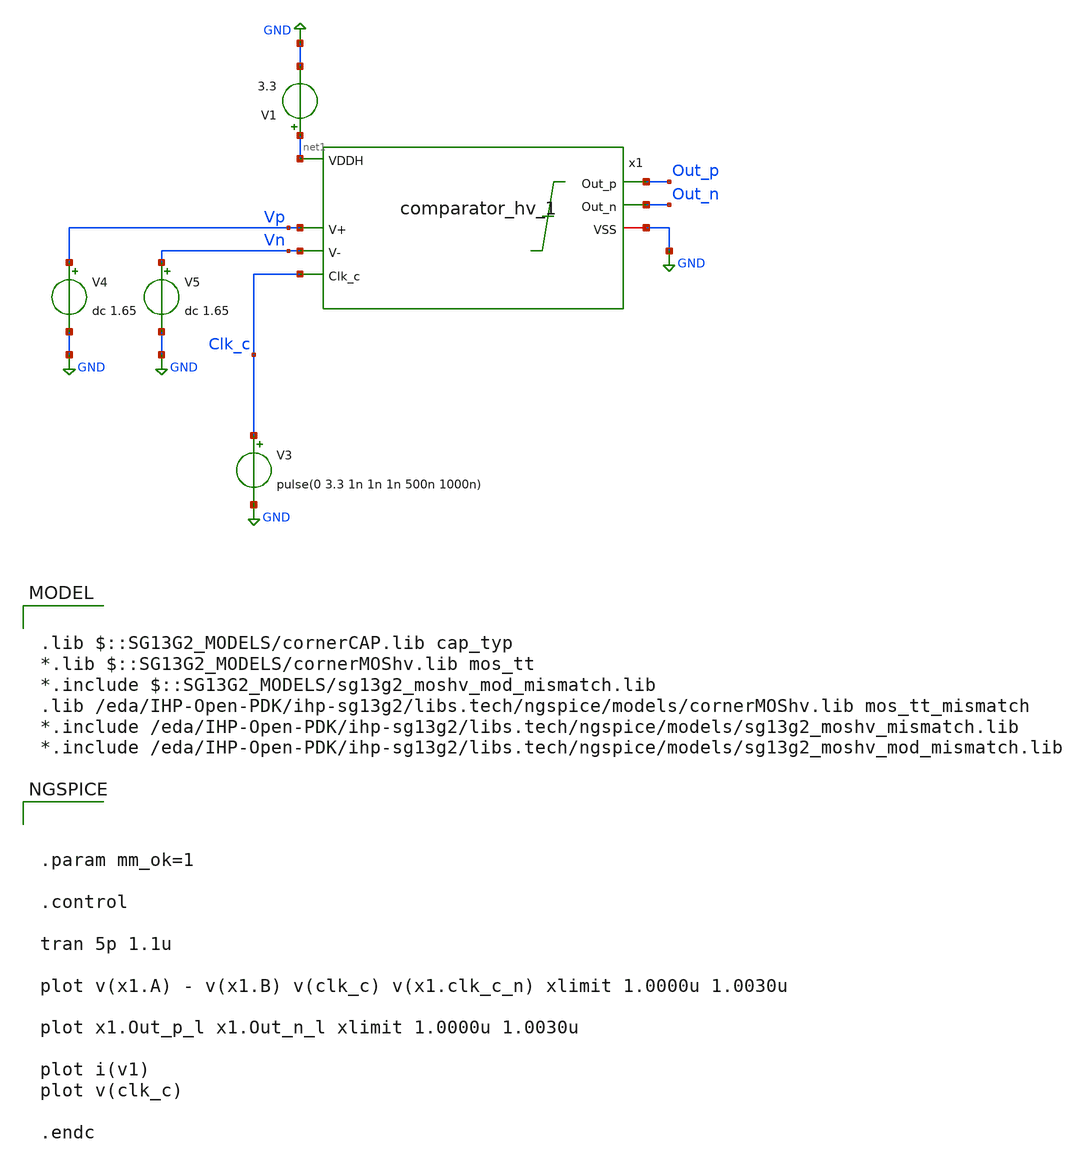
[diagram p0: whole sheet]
** sch_path: sar_adc/xschem/blocks/comparator/comparator_hv_tb.sch
**.subckt comparator_hv_tb
V3 Clk_c GND pulse(0 3.3 1n 1n 1n 500n 1000n)
V4 Vp GND dc 1.65
V5 Vn GND dc 1.65
V1 net1 GND 3.3
x1 net1 Vp Vn Out_p Out_n GND Clk_c comparator_hv_1
**** begin user architecture code

.lib $::SG13G2_MODELS/cornerCAP.lib cap_typ
*.lib $::SG13G2_MODELS/cornerMOShv.lib mos_tt
*.include $::SG13G2_MODELS/sg13g2_moshv_mod_mismatch.lib
.lib /eda/IHP-Open-PDK/ihp-sg13g2/libs.tech/ngspice/models/cornerMOShv.lib mos_tt_mismatch
*.include /eda/IHP-Open-PDK/ihp-sg13g2/libs.tech/ngspice/models/sg13g2_moshv_mismatch.lib
*.include /eda/IHP-Open-PDK/ihp-sg13g2/libs.tech/ngspice/models/sg13g2_moshv_mod_mismatch.lib




.param mm_ok=1

.control

tran 5p 1.1u

plot v(x1.A) - v(x1.B) v(clk_c) v(x1.clk_c_n) xlimit 1.0000u 1.0030u

plot x1.Out_p_l x1.Out_n_l xlimit 1.0000u 1.0030u

plot i(v1)
plot v(clk_c)

.endc


**** end user architecture code
**.ends
.GLOBAL GND
.end
